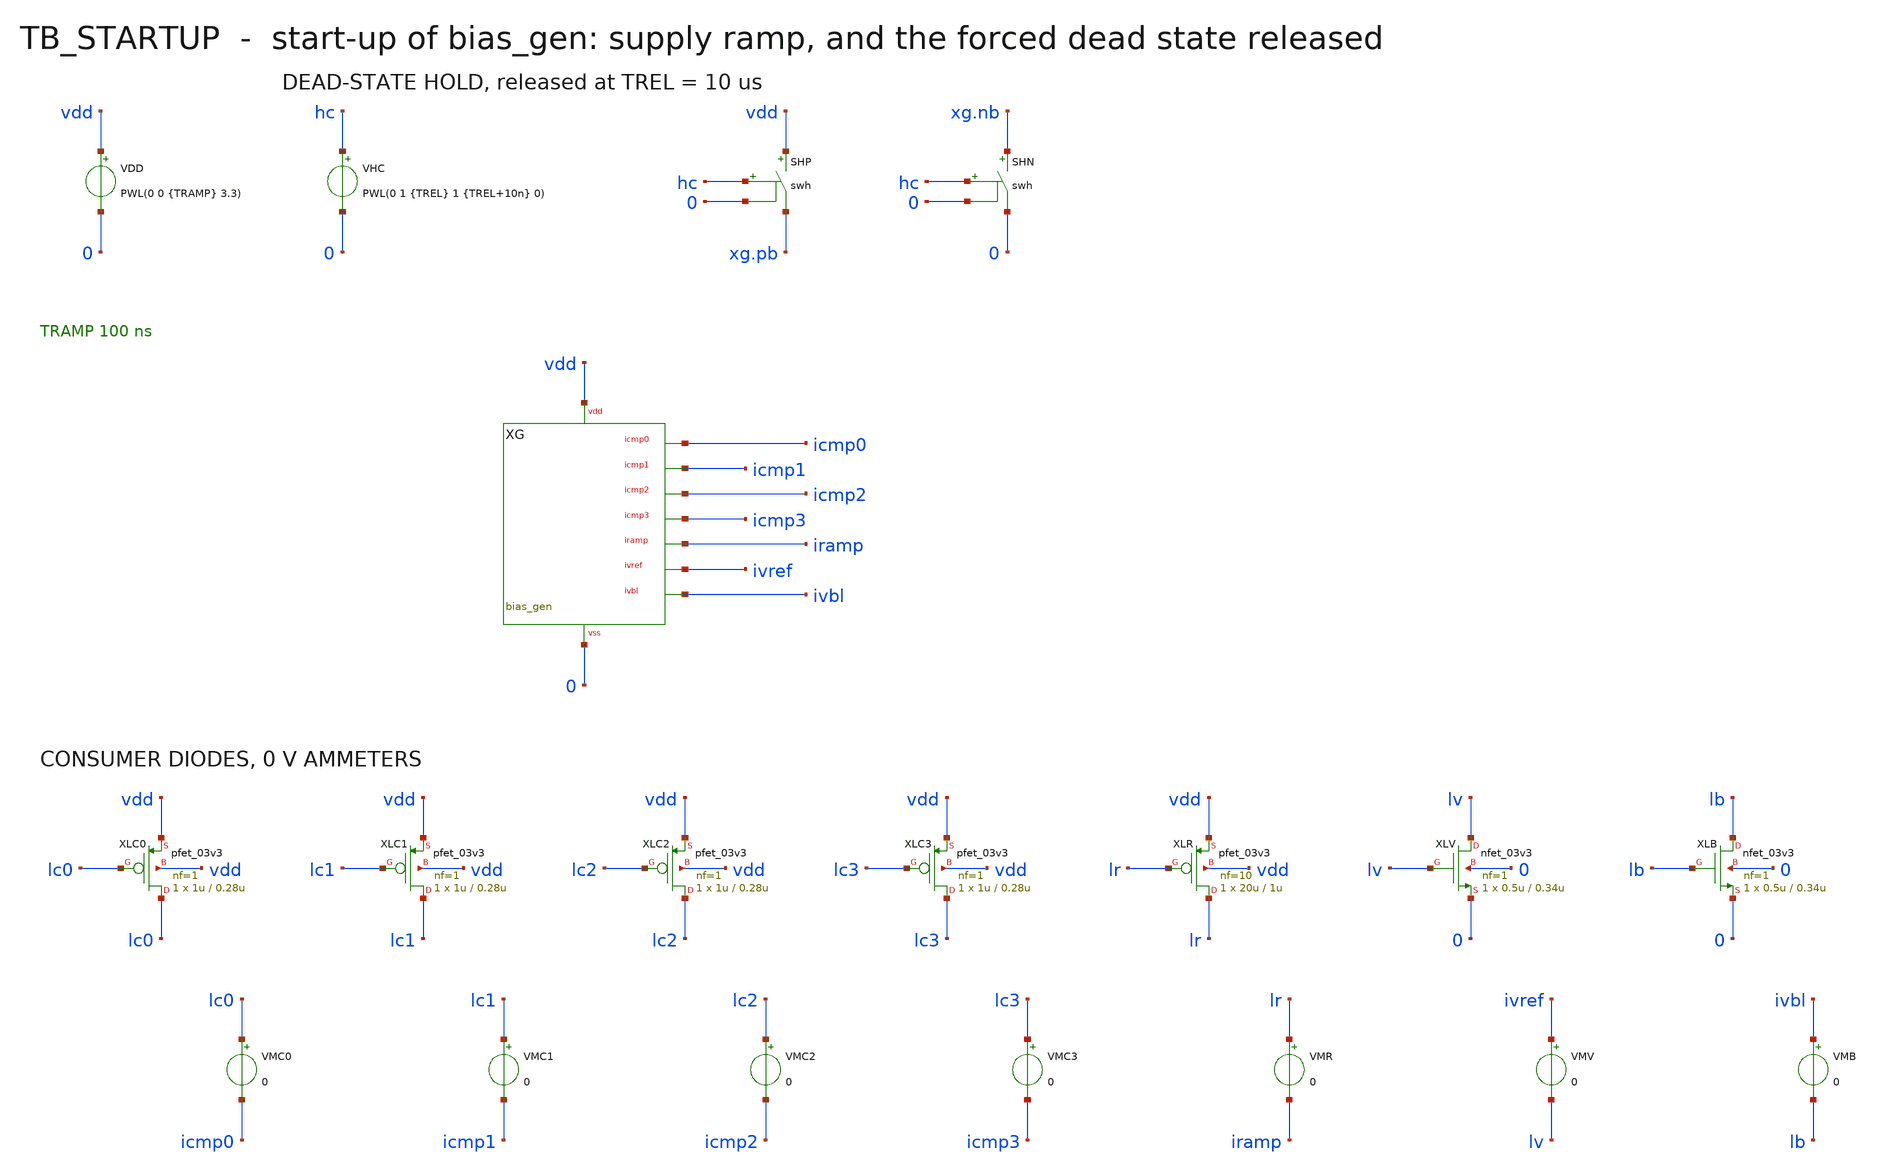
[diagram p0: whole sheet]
** sch_path: mixed_signal/bias_gen/tb_startup.sch
**.subckt tb_startup
VDD vdd 0 PWL(0 0 {TRAMP} 3.3)
VHC hc 0 PWL(0 1 {TREL} 1 {TREL+10n} 0)
SHP vdd xg.pb hc 0 swh
SHN xg.nb 0 hc 0 swh
XG vdd 0 icmp0 icmp1 icmp2 icmp3 iramp ivref ivbl bias_gen
XLC0 lc0 lc0 vdd vdd pfet_03v3 L=0.28u W=1u nf=1 m=1 ad=0.18p pd=2.36u as=0.18p ps=2.36u nrd=0.18
+ nrs=0.18
VMC0 lc0 icmp0 0
XLC1 lc1 lc1 vdd vdd pfet_03v3 L=0.28u W=1u nf=1 m=1 ad=0.18p pd=2.36u as=0.18p ps=2.36u nrd=0.18
+ nrs=0.18
VMC1 lc1 icmp1 0
XLC2 lc2 lc2 vdd vdd pfet_03v3 L=0.28u W=1u nf=1 m=1 ad=0.18p pd=2.36u as=0.18p ps=2.36u nrd=0.18
+ nrs=0.18
VMC2 lc2 icmp2 0
XLC3 lc3 lc3 vdd vdd pfet_03v3 L=0.28u W=1u nf=1 m=1 ad=0.18p pd=2.36u as=0.18p ps=2.36u nrd=0.18
+ nrs=0.18
VMC3 lc3 icmp3 0
XLR lr lr vdd vdd pfet_03v3 L=1u W=20u nf=10 m=1 ad=1.8p pd=21.8u as=2.16p ps=26.16u nrd=0.009
+ nrs=0.009
VMR lr iramp 0
XLV lv lv 0 0 nfet_03v3 L=0.34u W=0.5u nf=1 m=1 ad=0.09p pd=1.36u as=0.09p ps=1.36u nrd=0.36
+ nrs=0.36
VMV ivref lv 0
XLB lb lb 0 0 nfet_03v3 L=0.34u W=0.5u nf=1 m=1 ad=0.09p pd=1.36u as=0.09p ps=1.36u nrd=0.36
+ nrs=0.36
VMB ivbl lb 0
**** begin user architecture code

.include /foss/pdks/gf180mcuD/libs.tech/ngspice/design.ngspice
.lib /foss/pdks/gf180mcuD/libs.tech/ngspice/sm141064.ngspice typical
.lib /foss/pdks/gf180mcuD/libs.tech/ngspice/sm141064.ngspice res_typical
.lib /foss/pdks/gf180mcuD/libs.tech/ngspice/sm141064.ngspice mimcap_typical
.temp 27
.param TRAMP=100n
.param TREL=10u
.model swh sw vt=0.5 vh=0.1 ron=10 roff=1e15
.save all @m.xg.xmn1.m0[id]
.control
set num_threads=1
* case ramp100n: the supply ramps in TRAMP, the hold stays off
alter @vhc[pwl] = [ 0 0 1 0 ]
tran 5.025e-09 2.01e-05 0 5.025e-09 uic
meas tran icf find @m.xg.xmn1.m0[id] at=2.01e-05
meas tran icmpf find i(vmc0) at=2.01e-05
meas tran suf find v(xg.su) at=2.01e-05
echo START $&icf $&icmpf $&suf
let i90 = 0.9 * icf
meas tran t90 when @m.xg.xmn1.m0[id]=$&i90 rise=1
let tup = t90 - 1e-07
echo T90 $&tup
* case dead: settled supply, pb held at vdd and nb at 0 until TREL
alter @vdd[pwl] = [ 0 3.3 1 3.3 ]
alter @vhc[pwl] = [ 0 1 1e-05 1 1.001e-05 0 ]
tran 1.5e-08 6e-05 0 1.5e-08 uic
meas tran icf find @m.xg.xmn1.m0[id] at=6e-05
meas tran icmpf find i(vmc0) at=6e-05
meas tran suf find v(xg.su) at=6e-05
echo START $&icf $&icmpf $&suf
let i90 = 0.9 * icf
meas tran t90 when @m.xg.xmn1.m0[id]=$&i90 rise=1
let tup = t90 - 1e-05
echo T90 $&tup
quit
.endc

**** end user architecture code
**.ends
.end
